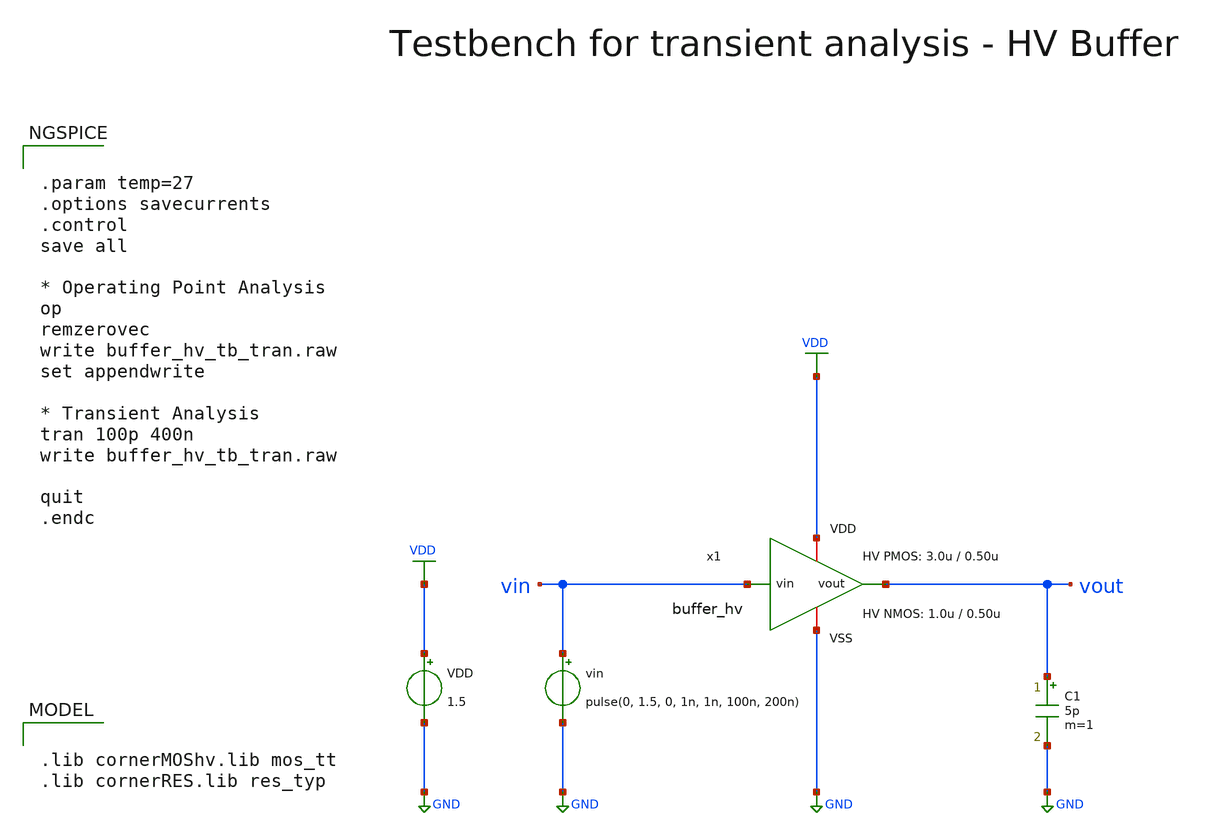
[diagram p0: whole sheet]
** sch_path: SG13G2_ATBS-ADC-main/xschem/buffer/testbenches/buffer_hv_tb_tran.sch
**.subckt buffer_hv_tb_tran
VDD VDD GND 1.5
vin vin GND pulse(0, 1.5, 0, 1n, 1n, 100n, 200n)
C1 vout GND 5p m=1
x1 VDD vin vout GND buffer_hv W_P_INV=3.0u L_P_INV=0.50u W_N_INV=1.0u L_N_INV=0.50u
**** begin user architecture code

.lib cornerMOShv.lib mos_tt
.lib cornerRES.lib res_typ



.param temp=27
.options savecurrents
.control
save all

* Operating Point Analysis
op
remzerovec
write buffer_hv_tb_tran.raw
set appendwrite

* Transient Analysis
tran 100p 400n
write buffer_hv_tb_tran.raw

quit
.endc


**** end user architecture code
**.ends

* expanding   symbol:  buffer/buffer_hv.sym # of pins=4
** sym_path: SG13G2_ATBS-ADC-main/xschem/buffer/buffer_hv.sym
** sch_path: SG13G2_ATBS-ADC-main/xschem/buffer/buffer_hv.sch
.subckt buffer_hv VDD vin vout VSS  W_P_INV=3.0u L_P_INV=0.50u W_N_INV=1.0u L_N_INV=0.50u
*.ipin vin
*.iopin VDD
*.iopin VSS
*.opin vout
x1 VDD vin net1 VSS inverter_hv W_P=W_P_INV L_P=L_P_INV W_N=W_N_INV L_N=L_N_INV
x2 VDD net1 vout VSS inverter_hv W_P=W_P_INV L_P=L_P_INV W_N=W_N_INV L_N=L_N_INV
.ends


* expanding   symbol:  inverter/inverter_hv.sym # of pins=4
** sym_path: SG13G2_ATBS-ADC-main/xschem/inverter/inverter_hv.sym
** sch_path: SG13G2_ATBS-ADC-main/xschem/inverter/inverter_hv.sch
.subckt inverter_hv VDD vin vout VSS  W_P=3.0u L_P=0.50u W_N=1.0u L_N=0.50u
*.ipin vin
*.iopin VDD
*.iopin VSS
*.opin vout
XM1 vout vin VDD VDD sg13_hv_pmos w=W_P l=L_P ng=1 m=1 mm_ok=1
XM2 vout vin VSS VSS sg13_hv_nmos w=W_N l=L_N ng=1 m=1 mm_ok=1
.ends

.GLOBAL GND
.GLOBAL VDD
.end
